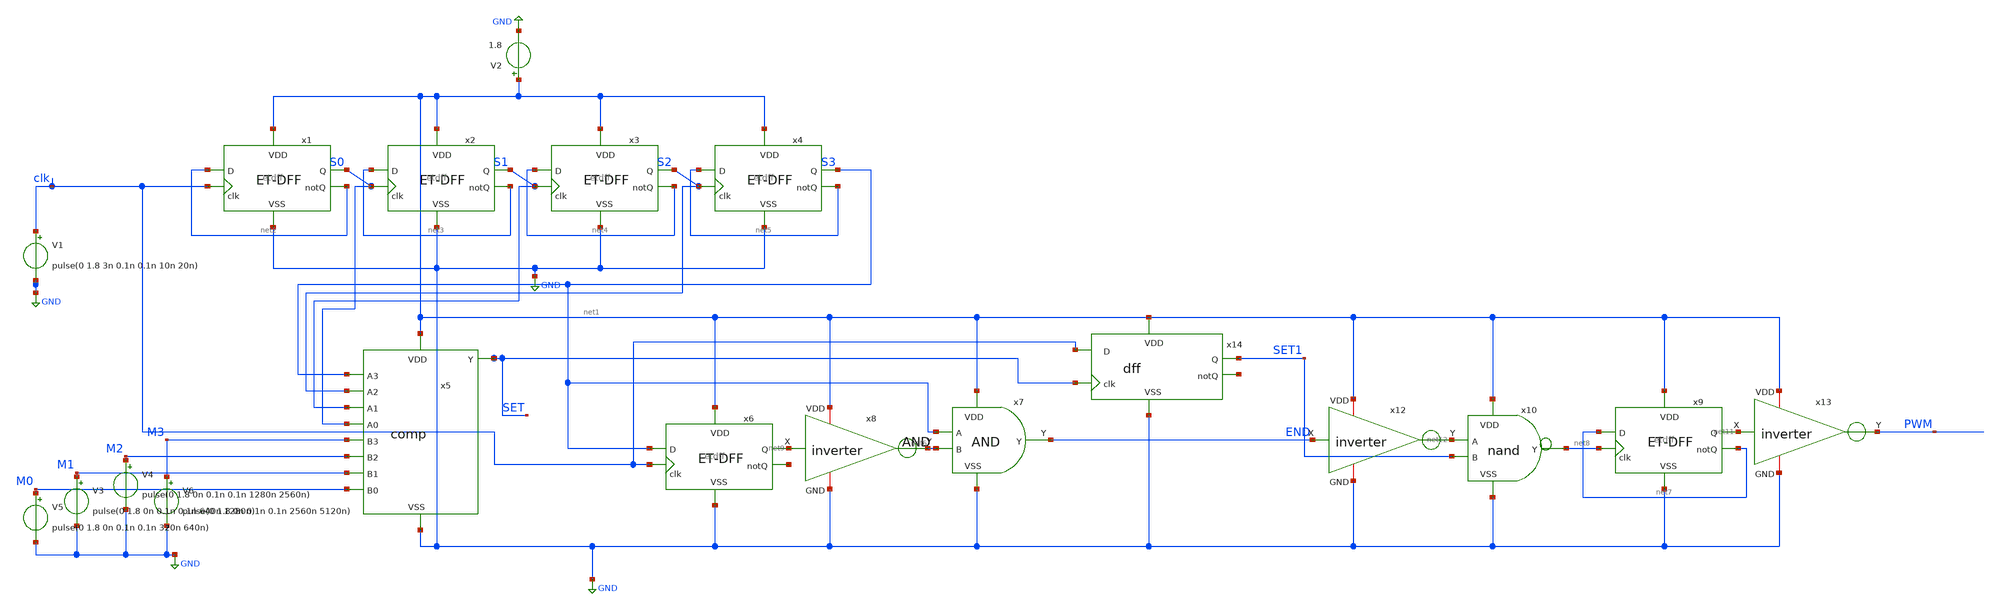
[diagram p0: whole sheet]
** sch_path: Layouts and Schematics/Spice Sim and Schem/pwmtest.sch
**.subckt pwmtest
V1 clk GND pulse(0 1.8 3n 0.1n 0.1n 10n 20n)
V2 net1 GND 1.8
V4 M2 GND pulse(0 1.8 0n 0.1n 0.1n 1280n 2560n)
V3 M1 GND pulse(0 1.8 0n 0.1n 0.1n 640n 1280n)
V5 M0 GND pulse(0 1.8 0n 0.1n 0.1n 320n 640n)
V6 M3 GND pulse(0 1.8 0n 0.1n 0.1n 2560n 5120n)
x1 net1 net2 S0 clk net2 GND etdff
x2 net1 net3 S1 S0 net3 GND etdff
x3 net1 net4 S2 S1 net4 GND etdff
x4 net1 net5 S3 S2 net5 GND etdff
x5 net1 S3 S1 S0 S2 M3 M2 M1 M0 SET GND comp
x6 net1 S3 net9 clk net10 GND etdff
x7 net1 S3 END net6 GND and
x8 net1 net9 net6 GND inv
x9 net1 net7 net11 net8 net7 GND etdff
x10 net1 net12 net8 SET1 GND nand
x12 net1 END net12 GND inv
x13 net1 net11 PWM GND inv
x14 net1 SET SET1 clk net13 GND dff
**** begin user architecture code
 .lib $::SKYWATER_MODELS/sky130.lib.spice tt

.include /home/wyatt/EE431
.tran 1n 4800n
.control
run
.endc

**** end user architecture code
**.ends
.GLOBAL GND
.end
